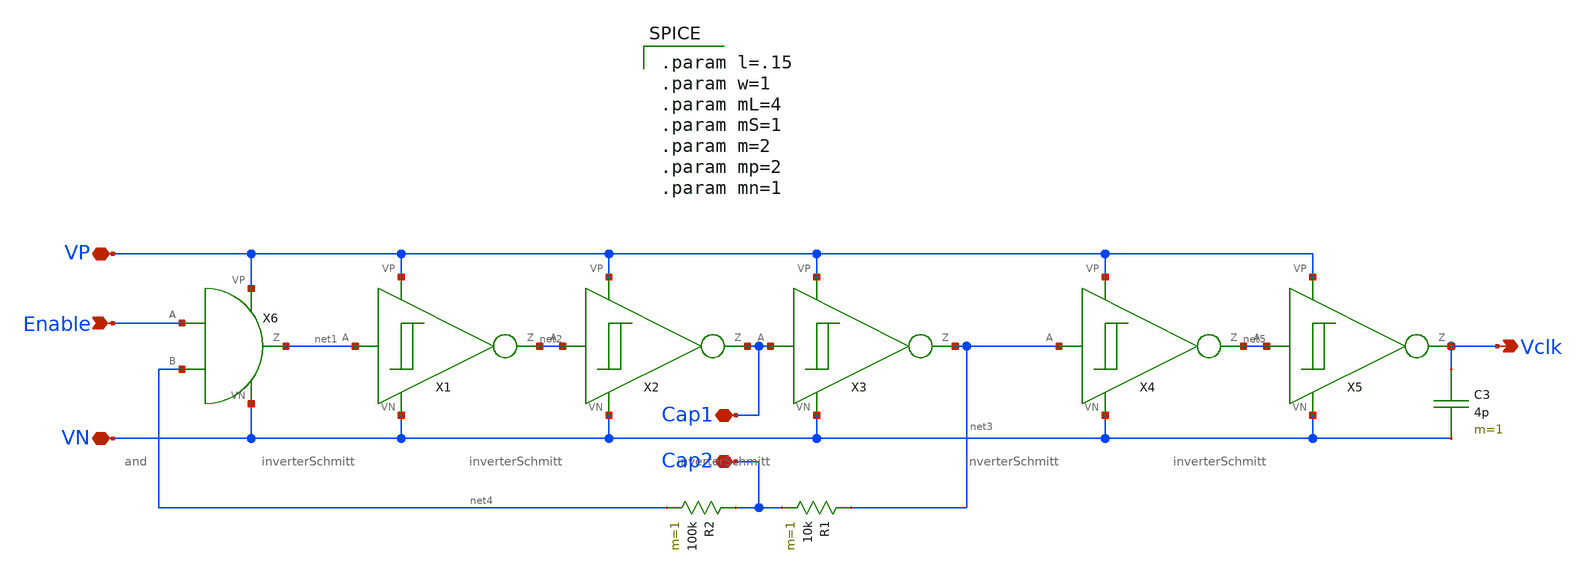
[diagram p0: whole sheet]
** sch_path: schematics/schmittOscillator.sch
**.subckt schmittOscillator Enable Cap1 Cap2 VP VN Vclk
*.ipin Enable
*.iopin Cap1
*.iopin Cap2
*.iopin VP
*.iopin VN
*.opin Vclk
X1 net1 VP VN net2 inverterSchmitt
X2 net2 VP VN Cap1 inverterSchmitt
X3 Cap1 VP VN net3 inverterSchmitt
R1 net3 Cap2 10k m=1
R2 Cap2 net4 100k m=1
X4 net3 VP VN net5 inverterSchmitt
X5 net5 VP VN Vclk inverterSchmitt
C3 Vclk VN 4p m=1
X6 Enable net4 VP VN net1 and
**** begin user architecture code

.param l=.15
.param w=1
.param mL=4
.param mS=1
.param m=2
.param mp=2
.param mn=1

**** end user architecture code
**.ends
.end
